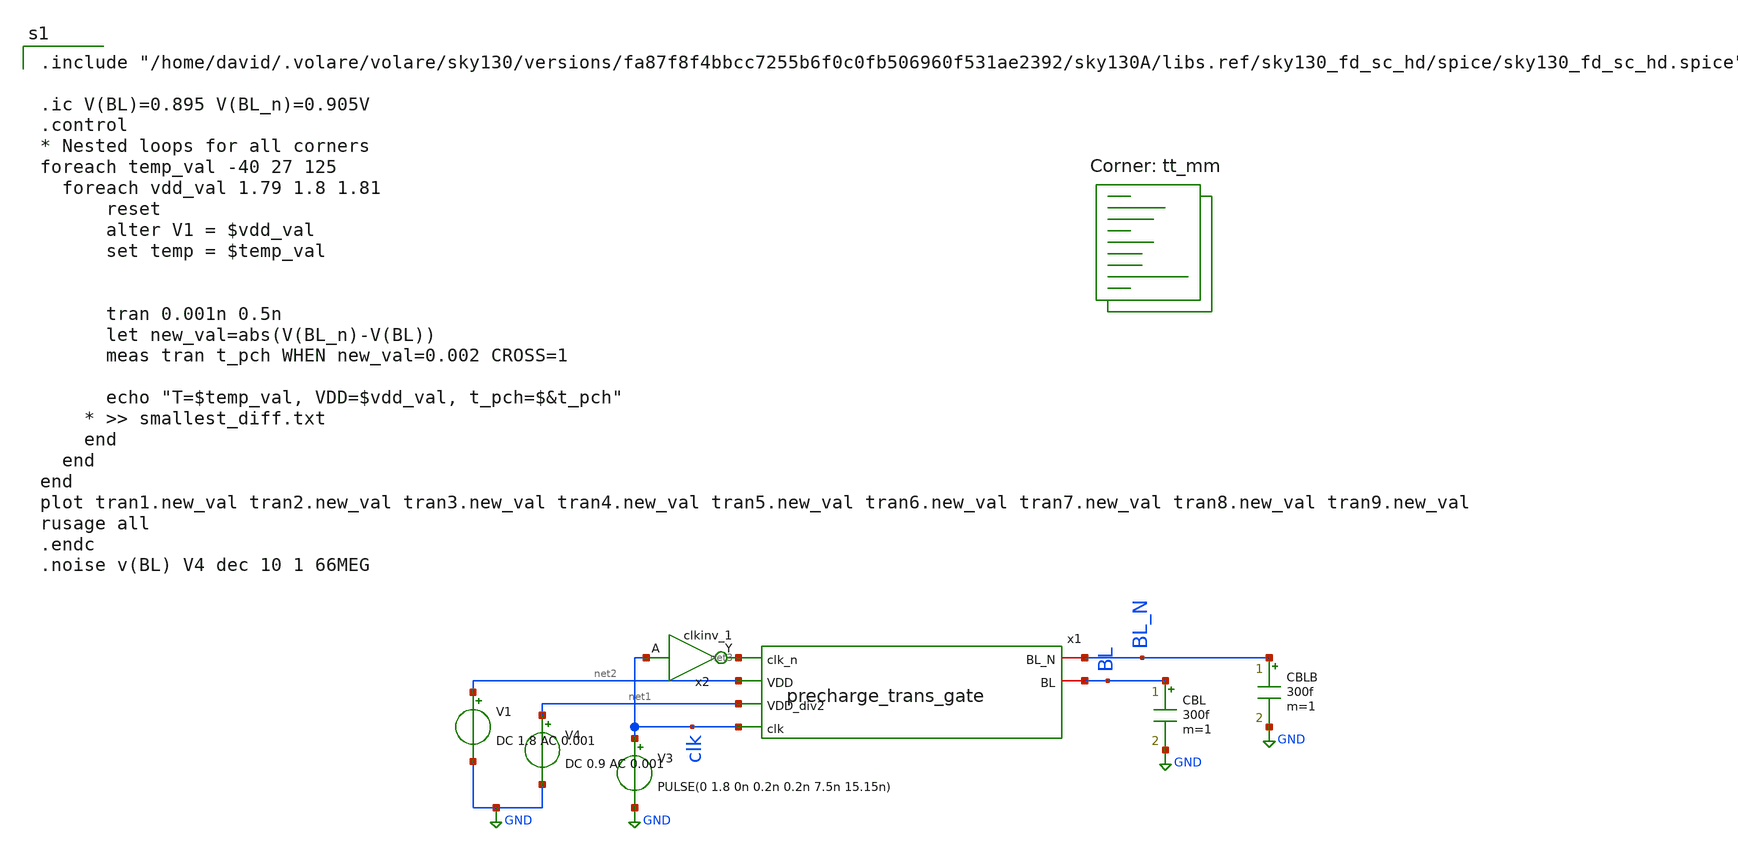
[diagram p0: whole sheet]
** sch_path: analog/schematics/trans_gate_tb.sch
**.subckt trans_gate_tb
V3 clk GND PULSE(0 1.8 0n 0.2n 0.2n 7.5n 15.15n)
x2 clk VGND VNB VPB VPWR net3 sky130_fd_sc_hd__clkinv_1
V4 net1 GND DC 0.9 AC 0.001
CBLB BL_N GND 300f m=1
CBL BL GND 300f m=1
x1 net3 BL_N BL net2 net1 clk precharge_trans_gate
V1 net2 GND DC 1.8 AC 0.001
**** begin user architecture code

.include "/home/david/.volare/volare/sky130/versions/fa87f8f4bbcc7255b6f0c0fb506960f531ae2392/sky130A/libs.ref/sky130_fd_sc_hd/spice/sky130_fd_sc_hd.spice"

.ic V(BL)=0.895 V(BL_n)=0.905V
.control
* Nested loops for all corners
foreach temp_val -40 27 125
  foreach vdd_val 1.79 1.8 1.81
      reset
      alter V1 = $vdd_val
      set temp = $temp_val


      tran 0.001n 0.5n
      let new_val=abs(V(BL_n)-V(BL))
      meas tran t_pch WHEN new_val=0.002 CROSS=1

      echo "T=$temp_val, VDD=$vdd_val, t_pch=$&t_pch"
    * >> smallest_diff.txt
    end
  end
end
plot tran1.new_val tran2.new_val tran3.new_val tran4.new_val tran5.new_val tran6.new_val
+ tran7.new_val tran8.new_val tran9.new_val
rusage all
.endc
.noise v(BL) V4 dec 10 1 66MEG

.lib $::SKYWATER_MODELS/sky130.lib.spice tt_mm
**** end user architecture code
**.ends
.GLOBAL GND
.end
